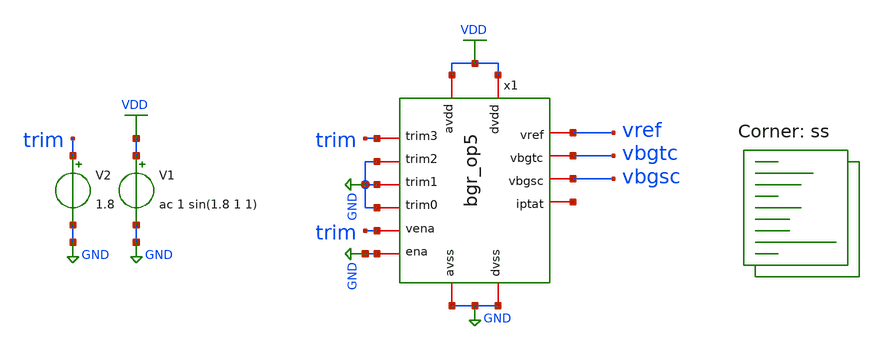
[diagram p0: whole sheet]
** sch_path: xschem/bgr_op5_tb.sch
**.subckt bgr_op5_tb
x1 net1 VDD vbgtc GND trim vbgsc GND GND GND trim GND VDD GND vref bgr_op5
V1 VDD GND ac 1 sin(1.8 1 1)
V2 trim GND 1.8
**** begin user architecture code


.option savecurrents
.control
save all
op
remzerovec
write bgr_op5_tb.raw

set appendwrite
set wr_singlescale
set wr_vecnames
option numdgt=3

dc temp -40 85 1
remzerovec
write bgr_op5_tb.raw
*write VREFFS.raw vref
*plot (ptat-ctat)
*plot ctat
plot vref
*wrdata vref5.csv vref
*plot vbgsc vbgtc

********TC********
meas dc temp_avg_vref avg v(vref)
meas dc temp_vref_27 find v(vref) when temp-sweep=27
meas dc temp_pp_vref PP v(vref)
meas dc temp_vref_max max v(vref)
meas dc temp_max_vref when v(vref)='temp_vref_max'
meas dc temp_vref_min min v(vref)
meas dc temp_min_vref when v(vref)='temp_vref_min'
let vref_tc='((temp_pp_vref*1000000)/(125*temp_avg_vref))'
print vref_tc

******PSRR******
ac dec 1000 1 10Meg
write bgr_op5_tb.raw
write PSRRFS.raw vdb(vref)
remzerovec
plot vdb(vref)
*wrdata PSRR5.csv vdb(vref)
meas ac psrr find vdb(vref) at=1k

****Power****
tran 10ms 500ms
write bgr_op5_tb.raw
set altshow
show >> bgr_op5.lis
remzerovec
meas tran ave_v avg vdd
meas tran ave_i avg i(v1)
let ave_power='ave_v*(-ave_i)
plot vdd vref
plot vg1 vgstart start
*plot -i(v1)
print ave_power

*******LS******
dc v1 0 3.5 0.05
write bgr_op5_tb.raw
remzerovec
plot vdd vref
meas dc vbg_27 find v(vref) at=1.8
meas dc vbgsc_27 find v(vbgsc) at=1.8
meas dc vbgtc_27 find v(vbgtc) at=1.8
meas dc vref_max max v(vref) from=1.62 to=1.98
meas dc vref_min min v(vref) from=1.62 to=1.98
let ls='(vref_max-vref_min)/(1.98-1.62)'
print ls

.endc


.lib $::SKYWATER_MODELS/sky130.lib.spice ss
**** end user architecture code
**.ends

* expanding   symbol:  bgr_op5.sym # of pins=14
** sym_path: xschem/bgr_op5.sym
** sch_path: xschem/bgr_op5.sch
.subckt bgr_op5 iptat avdd vbgtc ena vena vbgsc trim0 trim1 trim2 trim3 dvss dvdd avss vref
*.iopin ena
*.iopin vbgtc
*.iopin vbgsc
*.iopin vena
*.iopin avdd
*.iopin avss
*.iopin dvss
*.iopin trim0
*.iopin trim1
*.iopin trim2
*.iopin trim3
*.iopin dvdd
*.iopin vref
*.iopin iptat
XQ1 avss avss net1 sky130_fd_pr__pnp_05v5_W3p40L3p40 m=1
XQ2 avss avss ctat sky130_fd_pr__pnp_05v5_W3p40L3p40 m=8
**** begin user architecture code


.param L8=10
.param W8=1
.param L10=1
.param W10=1
.param R=492k


**** end user architecture code
Vctat start net1 0
.save i(vctat)
XM1 vref out vdde vdde sky130_fd_pr__pfet_01v8 L={L8} W={W8} nf=1 ad='int((nf+1)/2) * W/nf * 0.29' as='int((nf+2)/2)
+ * W/nf * 0.29' pd='2*int((nf+1)/2) * (W/nf + 0.29)' ps='2*int((nf+2)/2) * (W/nf + 0.29)' nrd='0.29 /
+ W' nrs='0.29 / W' sa=0 sb=0 sd=0 mult=4 m=4
XM2 net2 out vdde vdde sky130_fd_pr__pfet_01v8 L={L8} W={W8} nf=1 ad='int((nf+1)/2) * W/nf * 0.29' as='int((nf+2)/2)
+ * W/nf * 0.29' pd='2*int((nf+1)/2) * (W/nf + 0.29)' ps='2*int((nf+2)/2) * (W/nf + 0.29)' nrd='0.29 /
+ W' nrs='0.29 / W' sa=0 sb=0 sd=0 mult=4 m=4
Vctat1 net5 ctat 0
.save i(vctat1)
x2 net6 vref ptat net4 net3 avss Resistor492k_1
x3 net7 net2 start net8 net9 avss Resistor492k_1
x4 avss trim2 trim0 trim1 dvss net5 ptat trim3 Resistor50k_1
x5 vdde net10 net11 net12 avss Startup
XM3 vbgtc vena net4 DVSS sky130_fd_pr__nfet_01v8_lvt L=1 W=1 nf=1 ad='int((nf+1)/2) * W/nf * 0.29' as='int((nf+2)/2)
+ * W/nf * 0.29' pd='2*int((nf+1)/2) * (W/nf + 0.29)' ps='2*int((nf+2)/2) * (W/nf + 0.29)' nrd='0.29 /
+ W' nrs='0.29 / W' sa=0 sb=0 sd=0 mult=2 m=2
XM4 vbgsc vena net3 DVSS sky130_fd_pr__nfet_01v8_lvt L=1 W=1 nf=1 ad='int((nf+1)/2) * W/nf * 0.29' as='int((nf+2)/2)
+ * W/nf * 0.29' pd='2*int((nf+1)/2) * (W/nf + 0.29)' ps='2*int((nf+2)/2) * (W/nf + 0.29)' nrd='0.29 /
+ W' nrs='0.29 / W' sa=0 sb=0 sd=0 mult=2 m=2
XM5 iptat out vdde vdde sky130_fd_pr__pfet_01v8 L={L8} W={W8} nf=1 ad='int((nf+1)/2) * W/nf * 0.29' as='int((nf+2)/2)
+ * W/nf * 0.29' pd='2*int((nf+1)/2) * (W/nf + 0.29)' ps='2*int((nf+2)/2) * (W/nf + 0.29)' nrd='0.29 /
+ W' nrs='0.29 / W' sa=0 sb=0 sd=0 mult=4 m=4
x1 out vdde avss ptat start op5
XM6 vdde ena avdd DVDD sky130_fd_pr__pfet_01v8 L=2 W=2 nf=1 ad='int((nf+1)/2) * W/nf * 0.29' as='int((nf+2)/2)
+ * W/nf * 0.29' pd='2*int((nf+1)/2) * (W/nf + 0.29)' ps='2*int((nf+2)/2) * (W/nf + 0.29)' nrd='0.29 /
+ W' nrs='0.29 / W' sa=0 sb=0 sd=0 mult=4 m=4
.ends


* expanding   symbol:  Resistor492k_1.sym # of pins=6
** sym_path: xschem/Resistor492k_1.sym
** sch_path: xschem/Resistor492k_1.sch
.subckt Resistor492k_1 VBG A B VBGTC VBGSC avss
*.iopin A
*.iopin VBGTC
*.iopin B
*.iopin VBGSC
*.iopin VBG
*.iopin avss
XR1 net1 A avss sky130_fd_pr__res_high_po_0p35 L={L} mult=1 m=1
XR2 net2 net1 avss sky130_fd_pr__res_high_po_0p35 L={L} mult=1 m=1
XR3 VBG net2 avss sky130_fd_pr__res_high_po_0p35 L={L} mult=1 m=1
XR4 net3 VBG avss sky130_fd_pr__res_high_po_0p35 L={L} mult=1 m=1
XR5 net4 net3 avss sky130_fd_pr__res_high_po_0p35 L={L} mult=1 m=1
**** begin user architecture code


.param L=17


**** end user architecture code
XR6 net5 net6 avss sky130_fd_pr__res_high_po_0p35 L={L} mult=1 m=1
XR7 VBGSC net5 avss sky130_fd_pr__res_high_po_0p35 L={L} mult=1 m=1
XR8 VBGTC VBGSC avss sky130_fd_pr__res_high_po_0p35 L={L} mult=1 m=1
XR9 net7 VBGTC avss sky130_fd_pr__res_high_po_0p35 L={L} mult=1 m=1
XR10 net4 net7 avss sky130_fd_pr__res_high_po_0p35 L={L} mult=1 m=1
XR11 net8 net6 avss sky130_fd_pr__res_high_po_0p35 L={L} mult=1 m=1
XR12 net9 net8 avss sky130_fd_pr__res_high_po_0p35 L={L} mult=1 m=1
XR13 net11 net9 avss sky130_fd_pr__res_high_po_0p35 L={L} mult=1 m=1
XR14 net10 net11 avss sky130_fd_pr__res_high_po_0p35 L={L} mult=1 m=1
XR15 net12 net10 avss sky130_fd_pr__res_high_po_0p35 L={L} mult=1 m=1
XR16 net18 net13 avss sky130_fd_pr__res_high_po_0p35 L={L} mult=1 m=1
XR17 net14 net18 avss sky130_fd_pr__res_high_po_0p35 L={L} mult=1 m=1
XR18 net16 net14 avss sky130_fd_pr__res_high_po_0p35 L={L} mult=1 m=1
XR19 net15 net16 avss sky130_fd_pr__res_high_po_0p35 L={L} mult=1 m=1
XR20 net12 net15 avss sky130_fd_pr__res_high_po_0p35 L={L} mult=1 m=1
XR21 net17 net13 avss sky130_fd_pr__res_high_po_0p35 L={L} mult=1 m=1
XR22 B net17 avss sky130_fd_pr__res_high_po_0p35 L={L} mult=1 m=1
.ends


* expanding   symbol:  Resistor50k_1.sym # of pins=8
** sym_path: xschem/Resistor50k_1.sym
** sch_path: xschem/Resistor50k_1.sch
.subckt Resistor50k_1 avss trim2 trim0 trim1 dvss B A trim3
*.iopin A
*.iopin B
*.iopin avss
*.iopin dvss
*.iopin trim3
*.iopin trim2
*.iopin trim1
*.iopin trim0
XR2 net2 net1 avss sky130_fd_pr__res_high_po_0p35 L={L} mult=1 m=1
**** begin user architecture code


.param L=17
.param La=8.4
.param L1=1
.param W1=4


**** end user architecture code
XR3 A net2 avss sky130_fd_pr__res_high_po_0p35 L={L} mult=1 m=1
XR1 net1 net3 avss sky130_fd_pr__res_high_po_0p35 L={La} mult=2 m=2
XR4 net3 net4 avss sky130_fd_pr__res_high_po_0p35 L={La} mult=4 m=4
XR5 net4 net5 avss sky130_fd_pr__res_high_po_0p35 L={La} mult=8 m=8
XR6 net5 B avss sky130_fd_pr__res_high_po_0p35 L={La} mult=16 m=16
XM4 net1 trim3 net3 DVSS sky130_fd_pr__nfet_01v8_lvt L={L1} W={W1} nf=1 ad='int((nf+1)/2) * W/nf * 0.29' as='int((nf+2)/2)
+ * W/nf * 0.29' pd='2*int((nf+1)/2) * (W/nf + 0.29)' ps='2*int((nf+2)/2) * (W/nf + 0.29)' nrd='0.29 /
+ W' nrs='0.29 / W' sa=0 sb=0 sd=0 mult=4 m=4
XM1 net3 trim2 net4 DVSS sky130_fd_pr__nfet_01v8_lvt L={L1} W={W1} nf=1 ad='int((nf+1)/2) * W/nf * 0.29' as='int((nf+2)/2)
+ * W/nf * 0.29' pd='2*int((nf+1)/2) * (W/nf + 0.29)' ps='2*int((nf+2)/2) * (W/nf + 0.29)' nrd='0.29 /
+ W' nrs='0.29 / W' sa=0 sb=0 sd=0 mult=4 m=4
XM2 net4 trim1 net5 DVSS sky130_fd_pr__nfet_01v8_lvt L={L1} W={W1} nf=1 ad='int((nf+1)/2) * W/nf * 0.29' as='int((nf+2)/2)
+ * W/nf * 0.29' pd='2*int((nf+1)/2) * (W/nf + 0.29)' ps='2*int((nf+2)/2) * (W/nf + 0.29)' nrd='0.29 /
+ W' nrs='0.29 / W' sa=0 sb=0 sd=0 mult=4 m=4
XM3 net5 trim0 B DVSS sky130_fd_pr__nfet_01v8_lvt L={L1} W={W1} nf=1 ad='int((nf+1)/2) * W/nf * 0.29' as='int((nf+2)/2)
+ * W/nf * 0.29' pd='2*int((nf+1)/2) * (W/nf + 0.29)' ps='2*int((nf+2)/2) * (W/nf + 0.29)' nrd='0.29 /
+ W' nrs='0.29 / W' sa=0 sb=0 sd=0 mult=4 m=4
.ends


* expanding   symbol:  Startup.sym # of pins=5
** sym_path: xschem/Startup.sym
** sch_path: xschem/Startup.sch
.subckt Startup VDDE 2 1 out AVSS
*.iopin VDDE
*.iopin AVSS
*.iopin out
*.iopin 1
*.iopin 2
XM1 1 out AVSS AVSS sky130_fd_pr__nfet_01v8 L=1 W=1 nf=1 ad='int((nf+1)/2) * W/nf * 0.29' as='int((nf+2)/2)
+ * W/nf * 0.29' pd='2*int((nf+1)/2) * (W/nf + 0.29)' ps='2*int((nf+2)/2) * (W/nf + 0.29)' nrd='0.29 /
+ W' nrs='0.29 / W' sa=0 sb=0 sd=0 mult=4 m=4
XM2 2 1 VDDE VDDE sky130_fd_pr__pfet_01v8 L=10 W=1 nf=1 ad='int((nf+1)/2) * W/nf * 0.29' as='int((nf+2)/2)
+ * W/nf * 0.29' pd='2*int((nf+1)/2) * (W/nf + 0.29)' ps='2*int((nf+2)/2) * (W/nf + 0.29)' nrd='0.29 /
+ W' nrs='0.29 / W' sa=0 sb=0 sd=0 mult=1 m=1
XM3 1 1 VDDE VDDE sky130_fd_pr__pfet_01v8 L=10 W=1 nf=1 ad='int((nf+1)/2) * W/nf * 0.29' as='int((nf+2)/2)
+ * W/nf * 0.29' pd='2*int((nf+1)/2) * (W/nf + 0.29)' ps='2*int((nf+2)/2) * (W/nf + 0.29)' nrd='0.29 /
+ W' nrs='0.29 / W' sa=0 sb=0 sd=0 mult=1 m=1
XM4 out 2 VDDE VDDE sky130_fd_pr__pfet_01v8 L=10 W=1 nf=1 ad='int((nf+1)/2) * W/nf * 0.29' as='int((nf+2)/2)
+ * W/nf * 0.29' pd='2*int((nf+1)/2) * (W/nf + 0.29)' ps='2*int((nf+2)/2) * (W/nf + 0.29)' nrd='0.29 /
+ W' nrs='0.29 / W' sa=0 sb=0 sd=0 mult=1 m=1
x1 AVSS AVSS 2 ResistorStart
.ends


* expanding   symbol:  op5.sym # of pins=5
** sym_path: xschem/op5.sym
** sch_path: xschem/op5.sch
.subckt op5 out VDDE AVSS + -
*.iopin AVSS
*.iopin -
*.iopin +
*.iopin VDDE
*.iopin out
XM8 net1 net2 VDDE vdde sky130_fd_pr__pfet_01v8 L={L7} W={W7} nf=1 ad='int((nf+1)/2) * W/nf * 0.29' as='int((nf+2)/2)
+ * W/nf * 0.29' pd='2*int((nf+1)/2) * (W/nf + 0.29)' ps='2*int((nf+2)/2) * (W/nf + 0.29)' nrd='0.29 /
+ W' nrs='0.29 / W' sa=0 sb=0 sd=0 mult=2 m=2
XM9 net2 net2 VDDE vdde sky130_fd_pr__pfet_01v8 L={L7} W={W7} nf=1 ad='int((nf+1)/2) * W/nf * 0.29' as='int((nf+2)/2)
+ * W/nf * 0.29' pd='2*int((nf+1)/2) * (W/nf + 0.29)' ps='2*int((nf+2)/2) * (W/nf + 0.29)' nrd='0.29 /
+ W' nrs='0.29 / W' sa=0 sb=0 sd=0 mult=2 m=2
XM5 net3 bias AVSS AVSS sky130_fd_pr__nfet_01v8 L={L6} W={W6} nf=1 ad='int((nf+1)/2) * W/nf * 0.29' as='int((nf+2)/2)
+ * W/nf * 0.29' pd='2*int((nf+1)/2) * (W/nf + 0.29)' ps='2*int((nf+2)/2) * (W/nf + 0.29)' nrd='0.29 /
+ W' nrs='0.29 / W' sa=0 sb=0 sd=0 mult=2 m=2
XM10 out net1 VDDE vdde sky130_fd_pr__pfet_01v8 L={L2} W={W2} nf=1 ad='int((nf+1)/2) * W/nf * 0.29' as='int((nf+2)/2)
+ * W/nf * 0.29' pd='2*int((nf+1)/2) * (W/nf + 0.29)' ps='2*int((nf+2)/2) * (W/nf + 0.29)' nrd='0.29 /
+ W' nrs='0.29 / W' sa=0 sb=0 sd=0 mult=4 m=4
**** begin user architecture code


.include /home/gils/sky130_pdk/share/pdk/sky130A/libs.ref/sky130_fd_pr/spice/sky130_fd_pr__cap_vpp_11p5x11p7_l1m1m2m3_shieldm4.model.spice
**************
*PMOS cms
.param L1=10
.param W1=1

**************
*PMOS current differential
.param L7=10
.param W7=1

**************
*differential Pair
.param L4=13
.param W4=0.9

**************
*NMOS current control
.param L6=20
.param W6=1

**************
*Second Stage
.param L2=10
.param W2=1


**** end user architecture code
XM11 out bias AVSS AVSS sky130_fd_pr__nfet_01v8 L={L6} W={W6} nf=1 ad='int((nf+1)/2) * W/nf * 0.29' as='int((nf+2)/2)
+ * W/nf * 0.29' pd='2*int((nf+1)/2) * (W/nf + 0.29)' ps='2*int((nf+2)/2) * (W/nf + 0.29)' nrd='0.29 /
+ W' nrs='0.29 / W' sa=0 sb=0 sd=0 mult=2 m=2
XM3 net1 + net3 AVSS sky130_fd_pr__nfet_01v8 L={L4} W={W4} nf=1 ad='int((nf+1)/2) * W/nf * 0.29' as='int((nf+2)/2)
+ * W/nf * 0.29' pd='2*int((nf+1)/2) * (W/nf + 0.29)' ps='2*int((nf+2)/2) * (W/nf + 0.29)' nrd='0.29 /
+ W' nrs='0.29 / W' sa=0 sb=0 sd=0 mult=2 m=2
XM1 bias net6 VDDE vdde sky130_fd_pr__pfet_01v8 L={L1} W={W1} nf=1 ad='int((nf+1)/2) * W/nf * 0.29' as='int((nf+2)/2)
+ * W/nf * 0.29' pd='2*int((nf+1)/2) * (W/nf + 0.29)' ps='2*int((nf+2)/2) * (W/nf + 0.29)' nrd='0.29 /
+ W' nrs='0.29 / W' sa=0 sb=0 sd=0 mult=2 m=2
XM2 net6 net6 VDDE vdde sky130_fd_pr__pfet_01v8 L={L1} W={W1} nf=1 ad='int((nf+1)/2) * W/nf * 0.29' as='int((nf+2)/2)
+ * W/nf * 0.29' pd='2*int((nf+1)/2) * (W/nf + 0.29)' ps='2*int((nf+2)/2) * (W/nf + 0.29)' nrd='0.29 /
+ W' nrs='0.29 / W' sa=0 sb=0 sd=0 mult=2 m=2
XM6 net6 bias net7 AVSS sky130_fd_pr__nfet_01v8 L={L6} W={W6} nf=1 ad='int((nf+1)/2) * W/nf * 0.29' as='int((nf+2)/2)
+ * W/nf * 0.29' pd='2*int((nf+1)/2) * (W/nf + 0.29)' ps='2*int((nf+2)/2) * (W/nf + 0.29)' nrd='0.29 /
+ W' nrs='0.29 / W' sa=0 sb=0 sd=0 mult=2 m=2
XM7 bias bias AVSS AVSS sky130_fd_pr__nfet_01v8 L={L6} W={W6} nf=1 ad='int((nf+1)/2) * W/nf * 0.29' as='int((nf+2)/2)
+ * W/nf * 0.29' pd='2*int((nf+1)/2) * (W/nf + 0.29)' ps='2*int((nf+2)/2) * (W/nf + 0.29)' nrd='0.29 /
+ W' nrs='0.29 / W' sa=0 sb=0 sd=0 mult=2 m=2
XR4 net7 net8 AVSS sky130_fd_pr__res_high_po_0p35 L=4.5 mult=2 m=2
XM4 net2 - net3 AVSS sky130_fd_pr__nfet_01v8 L={L4} W={W4} nf=1 ad='int((nf+1)/2) * W/nf * 0.29' as='int((nf+2)/2)
+ * W/nf * 0.29' pd='2*int((nf+1)/2) * (W/nf + 0.29)' ps='2*int((nf+2)/2) * (W/nf + 0.29)' nrd='0.29 /
+ W' nrs='0.29 / W' sa=0 sb=0 sd=0 mult=2 m=2
XR1 net1 net4 AVSS sky130_fd_pr__res_high_po_0p35 L=4.5 mult=2 m=2
XR2 net4 net5 AVSS sky130_fd_pr__res_high_po_0p35 L=4.5 mult=2 m=2
XR9 net8 AVSS AVSS sky130_fd_pr__res_high_po_0p35 L=4.5 mult=2 m=2
XC1 net5 out sky130_fd_pr__cap_mim_m3_1 W=10 L=10 MF=4 m=4
.ends


* expanding   symbol:  ResistorStart.sym # of pins=3
** sym_path: xschem/ResistorStart.sym
** sch_path: xschem/ResistorStart.sch
.subckt ResistorStart AVSS B A
*.iopin A
*.iopin B
*.iopin AVSS
XR1 net1 A AVSS sky130_fd_pr__res_high_po_0p35 L=17 mult=1 m=1
XR2 net2 net1 AVSS sky130_fd_pr__res_high_po_0p35 L={L} mult=1 m=1
XR3 net4 net2 AVSS sky130_fd_pr__res_high_po_0p35 L={L} mult=1 m=1
XR4 net3 net4 AVSS sky130_fd_pr__res_high_po_0p35 L={L} mult=1 m=1
XR5 net5 net3 AVSS sky130_fd_pr__res_high_po_0p35 L={L} mult=1 m=1
**** begin user architecture code


.param L=17


**** end user architecture code
XR6 net6 net7 AVSS sky130_fd_pr__res_high_po_0p35 L={L} mult=1 m=1
XR7 net8 net6 AVSS sky130_fd_pr__res_high_po_0p35 L={L} mult=1 m=1
XR8 net10 net8 AVSS sky130_fd_pr__res_high_po_0p35 L={L} mult=1 m=1
XR9 net9 net10 AVSS sky130_fd_pr__res_high_po_0p35 L={L} mult=1 m=1
XR10 net5 net9 AVSS sky130_fd_pr__res_high_po_0p35 L={L} mult=1 m=1
XR11 net11 net7 AVSS sky130_fd_pr__res_high_po_0p35 L={L} mult=1 m=1
XR12 net12 net11 AVSS sky130_fd_pr__res_high_po_0p35 L={L} mult=1 m=1
XR13 net14 net12 AVSS sky130_fd_pr__res_high_po_0p35 L={L} mult=1 m=1
XR14 net13 net14 AVSS sky130_fd_pr__res_high_po_0p35 L={L} mult=1 m=1
XR15 net15 net13 AVSS sky130_fd_pr__res_high_po_0p35 L={L} mult=1 m=1
XR16 net16 net17 AVSS sky130_fd_pr__res_high_po_0p35 L={L} mult=1 m=1
XR17 net18 net16 AVSS sky130_fd_pr__res_high_po_0p35 L={L} mult=1 m=1
XR18 net20 net18 AVSS sky130_fd_pr__res_high_po_0p35 L={L} mult=1 m=1
XR19 net19 net20 AVSS sky130_fd_pr__res_high_po_0p35 L={L} mult=1 m=1
XR20 net15 net19 AVSS sky130_fd_pr__res_high_po_0p35 L={L} mult=1 m=1
XR21 net21 net17 AVSS sky130_fd_pr__res_high_po_0p35 L={L} mult=1 m=1
XR22 net22 net21 AVSS sky130_fd_pr__res_high_po_0p35 L={L} mult=1 m=1
XR23 net23 net22 AVSS sky130_fd_pr__res_high_po_0p35 L={L} mult=1 m=1
XR24 net24 net23 AVSS sky130_fd_pr__res_high_po_0p35 L={L} mult=1 m=1
XR25 net25 net24 AVSS sky130_fd_pr__res_high_po_0p35 L={L} mult=1 m=1
XR26 net26 B AVSS sky130_fd_pr__res_high_po_0p35 L={L} mult=1 m=1
XR27 net27 net26 AVSS sky130_fd_pr__res_high_po_0p35 L={L} mult=1 m=1
XR28 net28 net27 AVSS sky130_fd_pr__res_high_po_0p35 L={L} mult=1 m=1
XR29 net29 net28 AVSS sky130_fd_pr__res_high_po_0p35 L={L} mult=1 m=1
XR30 net25 net29 AVSS sky130_fd_pr__res_high_po_0p35 L={L} mult=1 m=1
.ends

.GLOBAL GND
.GLOBAL VDD
.end
